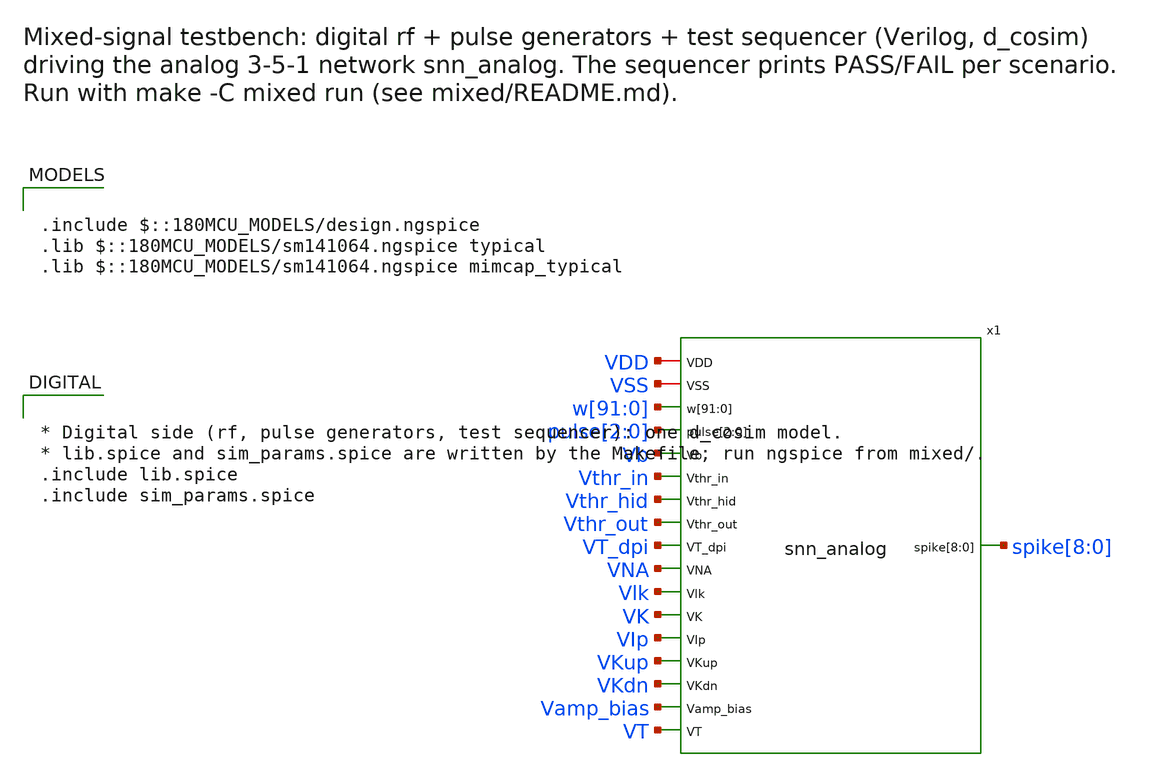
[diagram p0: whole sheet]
** sch_path: mixed/snn_ms_tb.sch
**.subckt snn_ms_tb
x1 VDD VSS w[91] w[90] w[89] w[88] w[87] w[86] w[85] w[84] w[83] w[82] w[81] w[80] w[79] w[78] w[77]
+ w[76] w[75] w[74] w[73] w[72] w[71] w[70] w[69] w[68] w[67] w[66] w[65] w[64] w[63] w[62] w[61] w[60]
+ w[59] w[58] w[57] w[56] w[55] w[54] w[53] w[52] w[51] w[50] w[49] w[48] w[47] w[46] w[45] w[44] w[43]
+ w[42] w[41] w[40] w[39] w[38] w[37] w[36] w[35] w[34] w[33] w[32] w[31] w[30] w[29] w[28] w[27] w[26]
+ w[25] w[24] w[23] w[22] w[21] w[20] w[19] w[18] w[17] w[16] w[15] w[14] w[13] w[12] w[11] w[10] w[9] w[8]
+ w[7] w[6] w[5] w[4] w[3] w[2] w[1] w[0] pulse[2] pulse[1] pulse[0] Vb Vthr_in Vthr_hid Vthr_out VT_dpi
+ VNA Vlk VK VIp VKup VKdn Vamp_bias VT spike[8] spike[7] spike[6] spike[5] spike[4] spike[3] spike[2]
+ spike[1] spike[0] snn_analog
**** begin user architecture code

.include $::180MCU_MODELS/design.ngspice
.lib $::180MCU_MODELS/sm141064.ngspice typical
.lib $::180MCU_MODELS/sm141064.ngspice mimcap_typical



* Digital side (rf, pulse generators, test sequencer): one d_cosim model.
* lib.spice and sim_params.spice are written by the Makefile; run ngspice from mixed/.
.include lib.spice
.include sim_params.spice




* Supplies and biases, as in analog/neuron/DACs-DPI-neuron.sch
* Parameter names start with p_: a .param with the same name as a net made ngspice
* rename that net to {name} on the long x1 line, leaving the biases unconnected.
.param p_vdd=3.3 p_vtau=0.40 p_iref=14.42n
.param p_vthr_in=2.909 p_vthr_hid=2.909 p_vthr_out=2.909
.param p_vlk=0.425 p_vamp_bias=0.535 p_vip=0.573 p_vna=1.93 p_vkup=2.35 p_vk=1.22 p_vkdn=0.588
+ p_vt=1.66
Vdd VDD 0 {p_vdd}
Vss VSS 0 0
* DAC unit current: Iref into a diode-connected unit current source (w[0] = 15 nA)
Iref VDD Vb {p_iref}
XMref Vb Vb 0 0 nfet_03v3 L=8u W=1u nf=1
Vthr_in Vthr_in 0 {p_vthr_in}
Vthr_hid Vthr_hid 0 {p_vthr_hid}
Vthr_out Vthr_out 0 {p_vthr_out}
Vtau VDD VT_dpi {p_vtau}
Vlk Vlk VSS {p_vlk}
VK VK VSS {p_vk}
VNA VNA VSS {p_vna}
VKup VKup VSS {p_vkup}
VKdn VKdn VSS {p_vkdn}
VIp VIp VSS {p_vip}
VT VT VSS {p_vt}
Vamp_bias Vamp_bias VSS {p_vamp_bias}
* Clocks: clk 1 us (rf, sequencer), clk_analog 10 us (pulse generators)
Vclk clk 0 pulse(0 {p_vdd} 0.5u 10n 10n 0.49u 1u)
Vclka clk_analog 0 pulse(0 {p_vdd} 5u 10n 10n 4.99u 10u)




* Gear integration: trap makes the DPI output current ring after each reset (entry 46)
.options method=gear
.csparam tstop_c={tstop}
.control
* Weights are not saved: they are static during a run and 92 traces made the .raw ~0.5 GB.
  save spike[0] spike[1] spike[2] spike[3] spike[4] spike[5] spike[6] spike[7] spike[8] pulse[0]
+ pulse[1] pulse[2] scen[0] scen[1] scen[2] running done x1.VMEM_0 x1.VMEM_1 x1.VMEM_2 x1.VMEM_3 x1.VMEM_4
+ x1.VMEM_5 x1.VMEM_6 x1.VMEM_7 x1.VMEM_8
  tran 0.5u $&tstop_c 0 0.5u
  write snn_ms_tb.raw
.endc


**** end user architecture code
**.ends
.end
